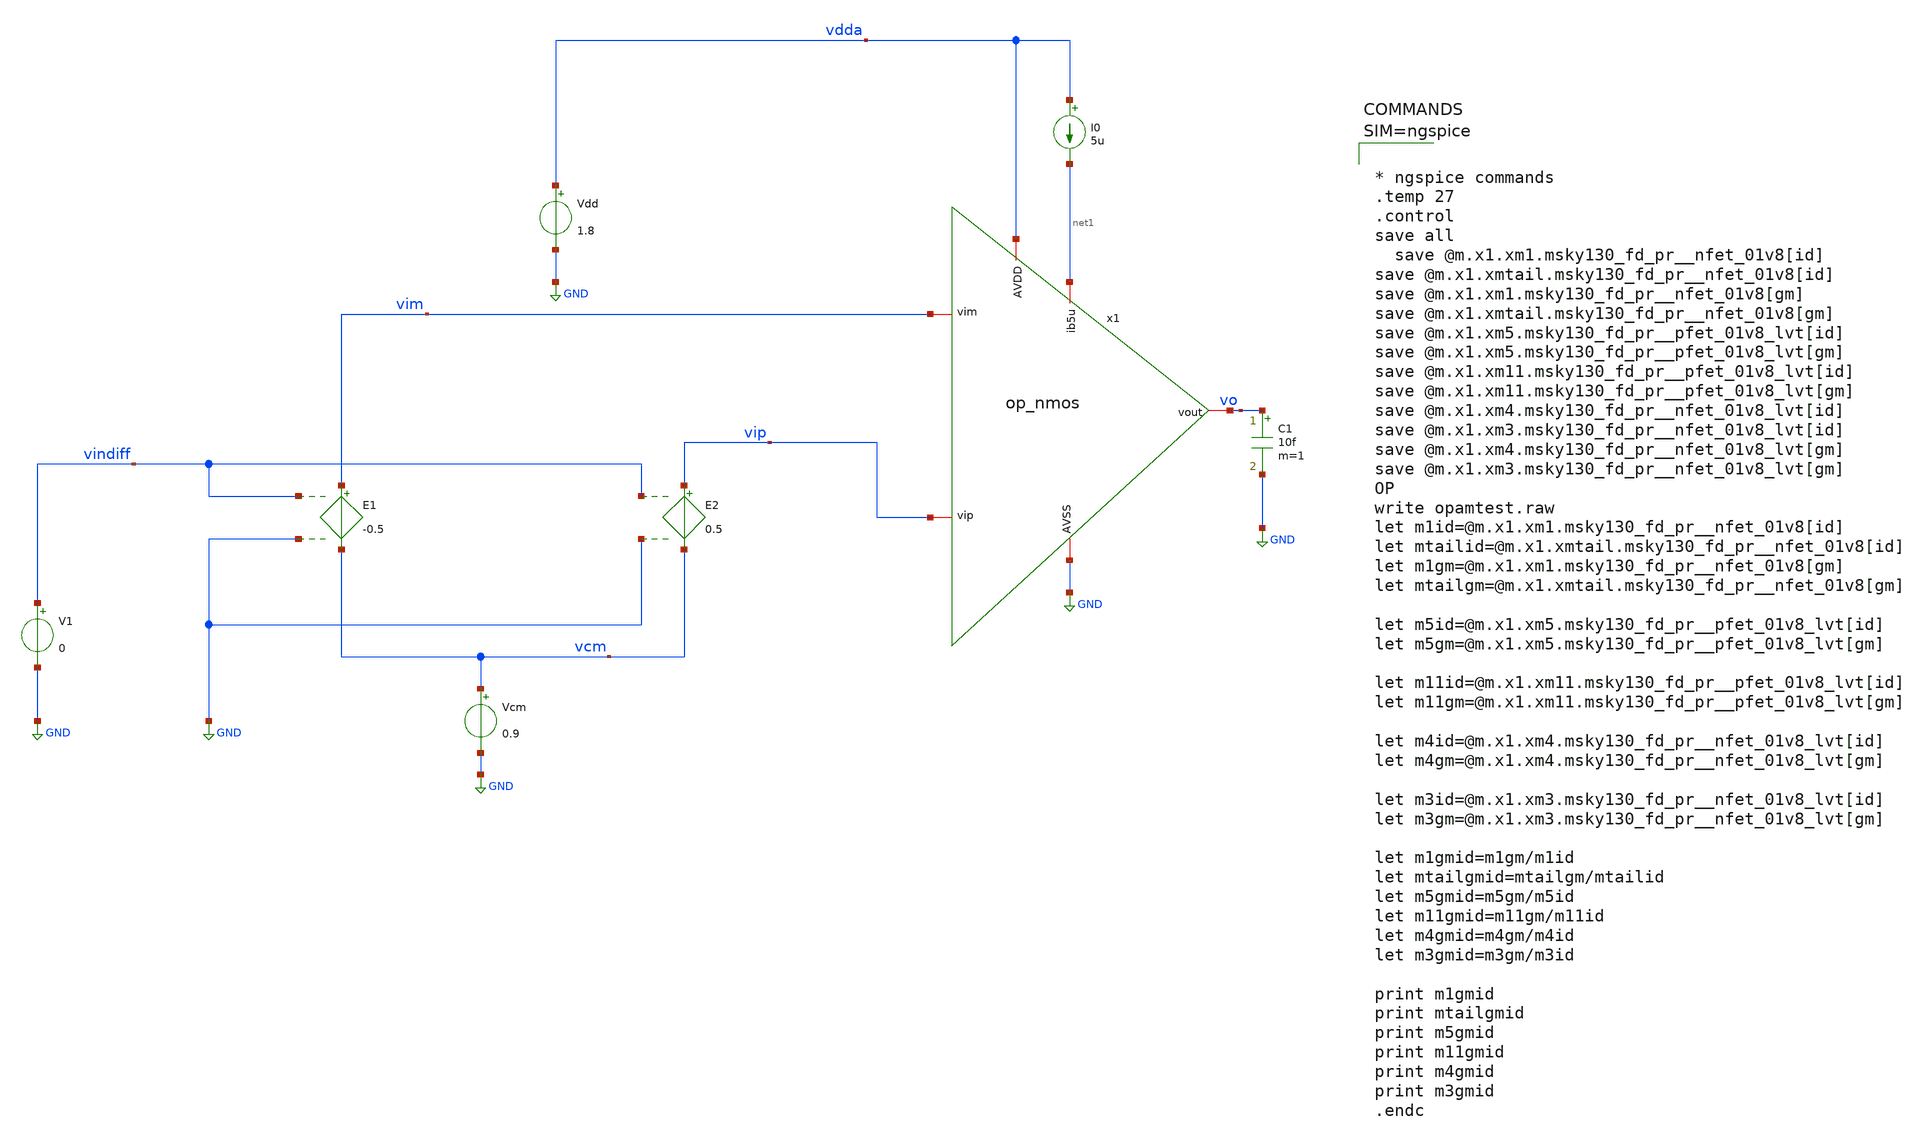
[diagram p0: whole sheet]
** sch_path: xschem/TB_op_nmos.sch
**.subckt TB_op_nmos
x1 vdda vo vim vip net1 GND op_nmos
E1 vim vcm vindiff GND -0.5
E2 vip vcm vindiff GND 0.5
V1 vindiff GND 0
Vcm vcm GND 0.9
Vdd vdda GND 1.8
C1 vo GND 10f m=1
I0 vdda net1 5u
**** begin user architecture code

** opencircuitdesign pdks install
.lib $::SKYWATER_MODELS/sky130.lib.spice tt




* ngspice commands
.temp 27
.control
save all
  save @m.x1.xm1.msky130_fd_pr__nfet_01v8[id]
save @m.x1.xmtail.msky130_fd_pr__nfet_01v8[id]
save @m.x1.xm1.msky130_fd_pr__nfet_01v8[gm]
save @m.x1.xmtail.msky130_fd_pr__nfet_01v8[gm]
save @m.x1.xm5.msky130_fd_pr__pfet_01v8_lvt[id]
save @m.x1.xm5.msky130_fd_pr__pfet_01v8_lvt[gm]
save @m.x1.xm11.msky130_fd_pr__pfet_01v8_lvt[id]
save @m.x1.xm11.msky130_fd_pr__pfet_01v8_lvt[gm]
save @m.x1.xm4.msky130_fd_pr__nfet_01v8_lvt[id]
save @m.x1.xm3.msky130_fd_pr__nfet_01v8_lvt[id]
save @m.x1.xm4.msky130_fd_pr__nfet_01v8_lvt[gm]
save @m.x1.xm3.msky130_fd_pr__nfet_01v8_lvt[gm]
OP
write opamtest.raw
let m1id=@m.x1.xm1.msky130_fd_pr__nfet_01v8[id]
let mtailid=@m.x1.xmtail.msky130_fd_pr__nfet_01v8[id]
let m1gm=@m.x1.xm1.msky130_fd_pr__nfet_01v8[gm]
let mtailgm=@m.x1.xmtail.msky130_fd_pr__nfet_01v8[gm]

let m5id=@m.x1.xm5.msky130_fd_pr__pfet_01v8_lvt[id]
let m5gm=@m.x1.xm5.msky130_fd_pr__pfet_01v8_lvt[gm]

let m11id=@m.x1.xm11.msky130_fd_pr__pfet_01v8_lvt[id]
let m11gm=@m.x1.xm11.msky130_fd_pr__pfet_01v8_lvt[gm]

let m4id=@m.x1.xm4.msky130_fd_pr__nfet_01v8_lvt[id]
let m4gm=@m.x1.xm4.msky130_fd_pr__nfet_01v8_lvt[gm]

let m3id=@m.x1.xm3.msky130_fd_pr__nfet_01v8_lvt[id]
let m3gm=@m.x1.xm3.msky130_fd_pr__nfet_01v8_lvt[gm]

let m1gmid=m1gm/m1id
let mtailgmid=mtailgm/mtailid
let m5gmid=m5gm/m5id
let m11gmid=m11gm/m11id
let m4gmid=m4gm/m4id
let m3gmid=m3gm/m3id

print m1gmid
print mtailgmid
print m5gmid
print m11gmid
print m4gmid
print m3gmid
.endc



**** end user architecture code
**.ends

* expanding   symbol:  op_nmos.sym # of pins=6
** sym_path: xschem/op_nmos.sym
** sch_path: xschem/op_nmos.sch
.subckt op_nmos AVDD vout vim vip ib5u AVSS
*.iopin ib5u
*.iopin AVSS
*.iopin vim
*.iopin vip
*.iopin AVDD
*.iopin vout
XM1 ib5u ib5u AVSS AVSS sky130_fd_pr__nfet_01v8 L=1 W=5 nf=1 ad='int((1 + 1)/2) * 5 / 1 * 0.29' as='int((1 + 2)/2) * 5 / 1 * 0.29'
+ pd='2*int((1 + 1)/2) * (5 / 1 + 0.29)' ps='2*int((1 + 2)/2) * (5 / 1 + 0.29)' nrd='0.29 / 5 ' nrs='0.29 / 5 '
+ sa=0 sb=0 sd=0 mult=1 m=1
XMtail net1 ib5u AVSS AVSS sky130_fd_pr__nfet_01v8 L=1 W=5 nf=1 ad='int((1 + 1)/2) * 5 / 1 * 0.29' as='int((1 + 2)/2) * 5 / 1 * 0.29'
+ pd='2*int((1 + 1)/2) * (5 / 1 + 0.29)' ps='2*int((1 + 2)/2) * (5 / 1 + 0.29)' nrd='0.29 / 5 ' nrs='0.29 / 5 '
+ sa=0 sb=0 sd=0 mult=1 m=1
XMip vom vip net1 net1 sky130_fd_pr__nfet_01v8_lvt L=2 W=5 nf=1 ad='int((1 + 1)/2) * 5 / 1 * 0.29' as='int((1 + 2)/2) * 5 / 1 * 0.29'
+ pd='2*int((1 + 1)/2) * (5 / 1 + 0.29)' ps='2*int((1 + 2)/2) * (5 / 1 + 0.29)' nrd='0.29 / 5 ' nrs='0.29 / 5 '
+ sa=0 sb=0 sd=0 mult=4 m=4
XMim vout vim net1 net1 sky130_fd_pr__nfet_01v8_lvt L=2 W=5 nf=1 ad='int((1 + 1)/2) * 5 / 1 * 0.29' as='int((1 + 2)/2) * 5 / 1 * 0.29'
+ pd='2*int((1 + 1)/2) * (5 / 1 + 0.29)' ps='2*int((1 + 2)/2) * (5 / 1 + 0.29)' nrd='0.29 / 5 ' nrs='0.29 / 5 '
+ sa=0 sb=0 sd=0 mult=4 m=4
XMpcmp vom vom AVDD AVDD sky130_fd_pr__pfet_01v8_lvt L=2 W=5 nf=1 ad='int((1 + 1)/2) * 5 / 1 * 0.29'
+ as='int((1 + 2)/2) * 5 / 1 * 0.29' pd='2*int((1 + 1)/2) * (5 / 1 + 0.29)' ps='2*int((1 + 2)/2) * (5 / 1 + 0.29)'
+ nrd='0.29 / 5 ' nrs='0.29 / 5 ' sa=0 sb=0 sd=0 mult=2 m=2
XMpcmm vout vom AVDD AVDD sky130_fd_pr__pfet_01v8_lvt L=2 W=5 nf=1 ad='int((1 + 1)/2) * 5 / 1 * 0.29'
+ as='int((1 + 2)/2) * 5 / 1 * 0.29' pd='2*int((1 + 1)/2) * (5 / 1 + 0.29)' ps='2*int((1 + 2)/2) * (5 / 1 + 0.29)'
+ nrd='0.29 / 5 ' nrs='0.29 / 5 ' sa=0 sb=0 sd=0 mult=2 m=2
.ends

.GLOBAL GND
.end
